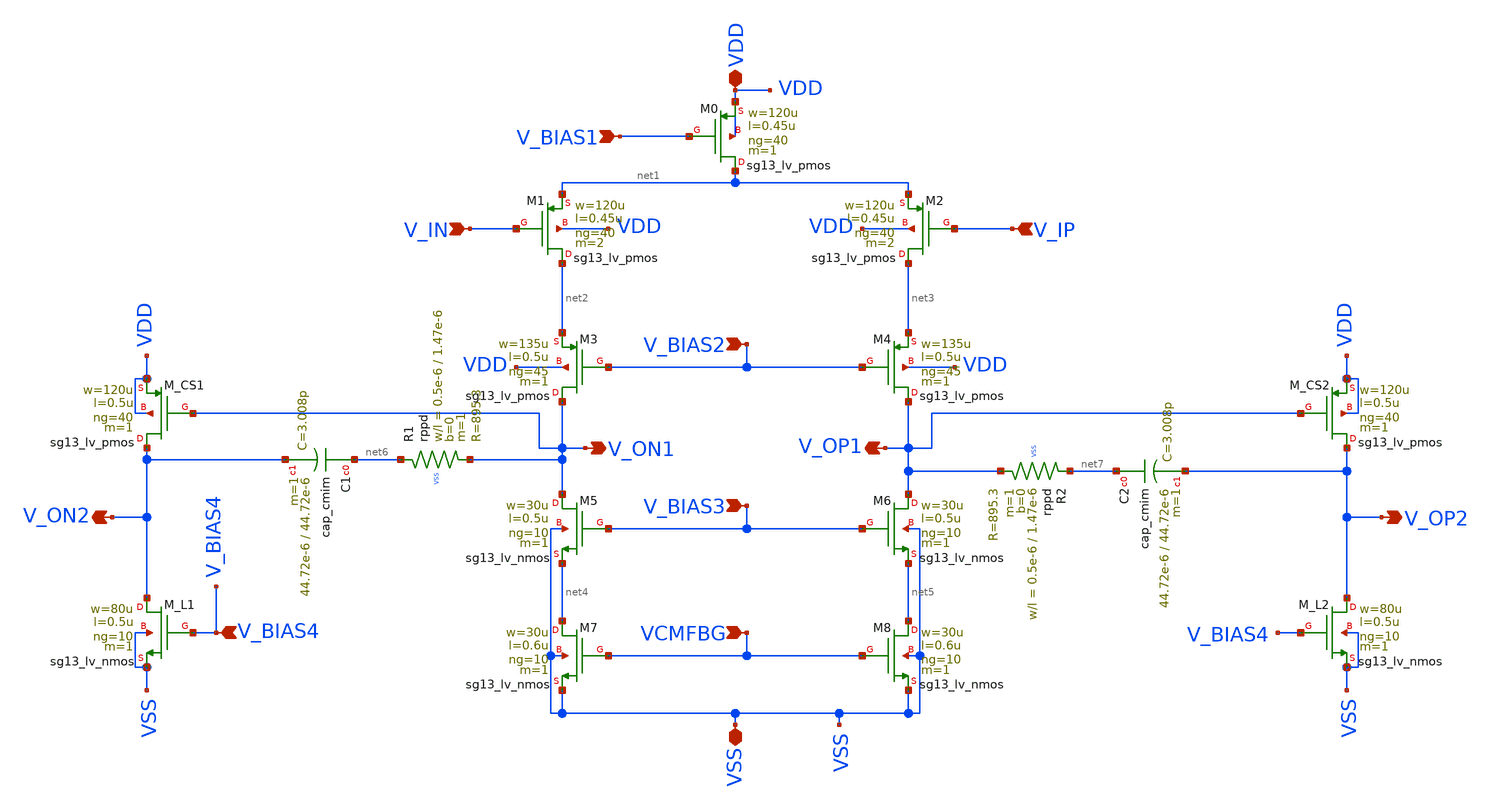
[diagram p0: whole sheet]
** sch_path: two-stage-ota-with-cmfb/Layout_PEX_PostSimulation/LAYOUT/SCHEMATIC_FOR_LAYOUT/CASCODE_Block/CASCODE_Block.sch
**.subckt CASCODE_Block VDD V_IN V_IP VSS V_BIAS2 V_BIAS1 VCMFBG V_ON1 V_OP1 V_BIAS3 V_BIAS4 V_ON2
*+ V_OP2
*.iopin VDD
*.ipin V_IN
*.ipin V_IP
*.iopin VSS
*.ipin V_BIAS2
*.ipin V_BIAS1
*.ipin VCMFBG
*.opin V_ON1
*.opin V_OP1
*.ipin V_BIAS3
*.ipin V_BIAS4
*.opin V_ON2
*.opin V_OP2
XM5 V_ON1 V_BIAS3 net4 VSS sg13_lv_nmos w=30u l=0.5u ng=10 m=1 mm_ok=1
XM6 V_OP1 V_BIAS3 net5 VSS sg13_lv_nmos w=30u l=0.5u ng=10 m=1 mm_ok=1
XM7 net4 VCMFBG VSS VSS sg13_lv_nmos w=30u l=0.6u ng=10 m=1 mm_ok=1
XM8 net5 VCMFBG VSS VSS sg13_lv_nmos w=30u l=0.6u ng=10 m=1 mm_ok=1
XM1 net2 V_IN net1 VDD sg13_lv_pmos w=120u l=0.45u ng=40 m=2 mm_ok=1
XM2 net3 V_IP net1 VDD sg13_lv_pmos w=120u l=0.45u ng=40 m=2 mm_ok=1
XM3 V_ON1 V_BIAS2 net2 VDD sg13_lv_pmos w=135u l=0.5u ng=45 m=1 mm_ok=1
XM4 V_OP1 V_BIAS2 net3 VDD sg13_lv_pmos w=135u l=0.5u ng=45 m=1 mm_ok=1
XM0 net1 V_BIAS1 VDD VDD sg13_lv_pmos w=120u l=0.45u ng=40 m=1 mm_ok=1
XM_CS1 V_ON2 V_ON1 VDD VDD sg13_lv_pmos w=120u l=0.5u ng=40 m=1 mm_ok=1
XM_CS2 V_OP2 V_OP1 VDD VDD sg13_lv_pmos w=120u l=0.5u ng=40 m=1 mm_ok=1
XM_L1 V_ON2 V_BIAS4 VSS VSS sg13_lv_nmos w=80u l=0.5u ng=10 m=1 mm_ok=1
XM_L2 V_OP2 V_BIAS4 VSS VSS sg13_lv_nmos w=80u l=0.5u ng=10 m=1 mm_ok=1
XC1 net6 V_ON2 cap_cmim w=44.72e-6 l=44.72e-6 m=1 mm_ok=1
XC2 net7 V_OP2 cap_cmim w=44.72e-6 l=44.72e-6 m=1 mm_ok=1
XR1 net6 V_ON1 VSS rppd w=0.5e-6 l=1.47e-6 m=1 b=0 mm_ok=1
XR2 net7 V_OP1 VSS rppd w=0.5e-6 l=1.47e-6 m=1 b=0 mm_ok=1
**.ends
.end
